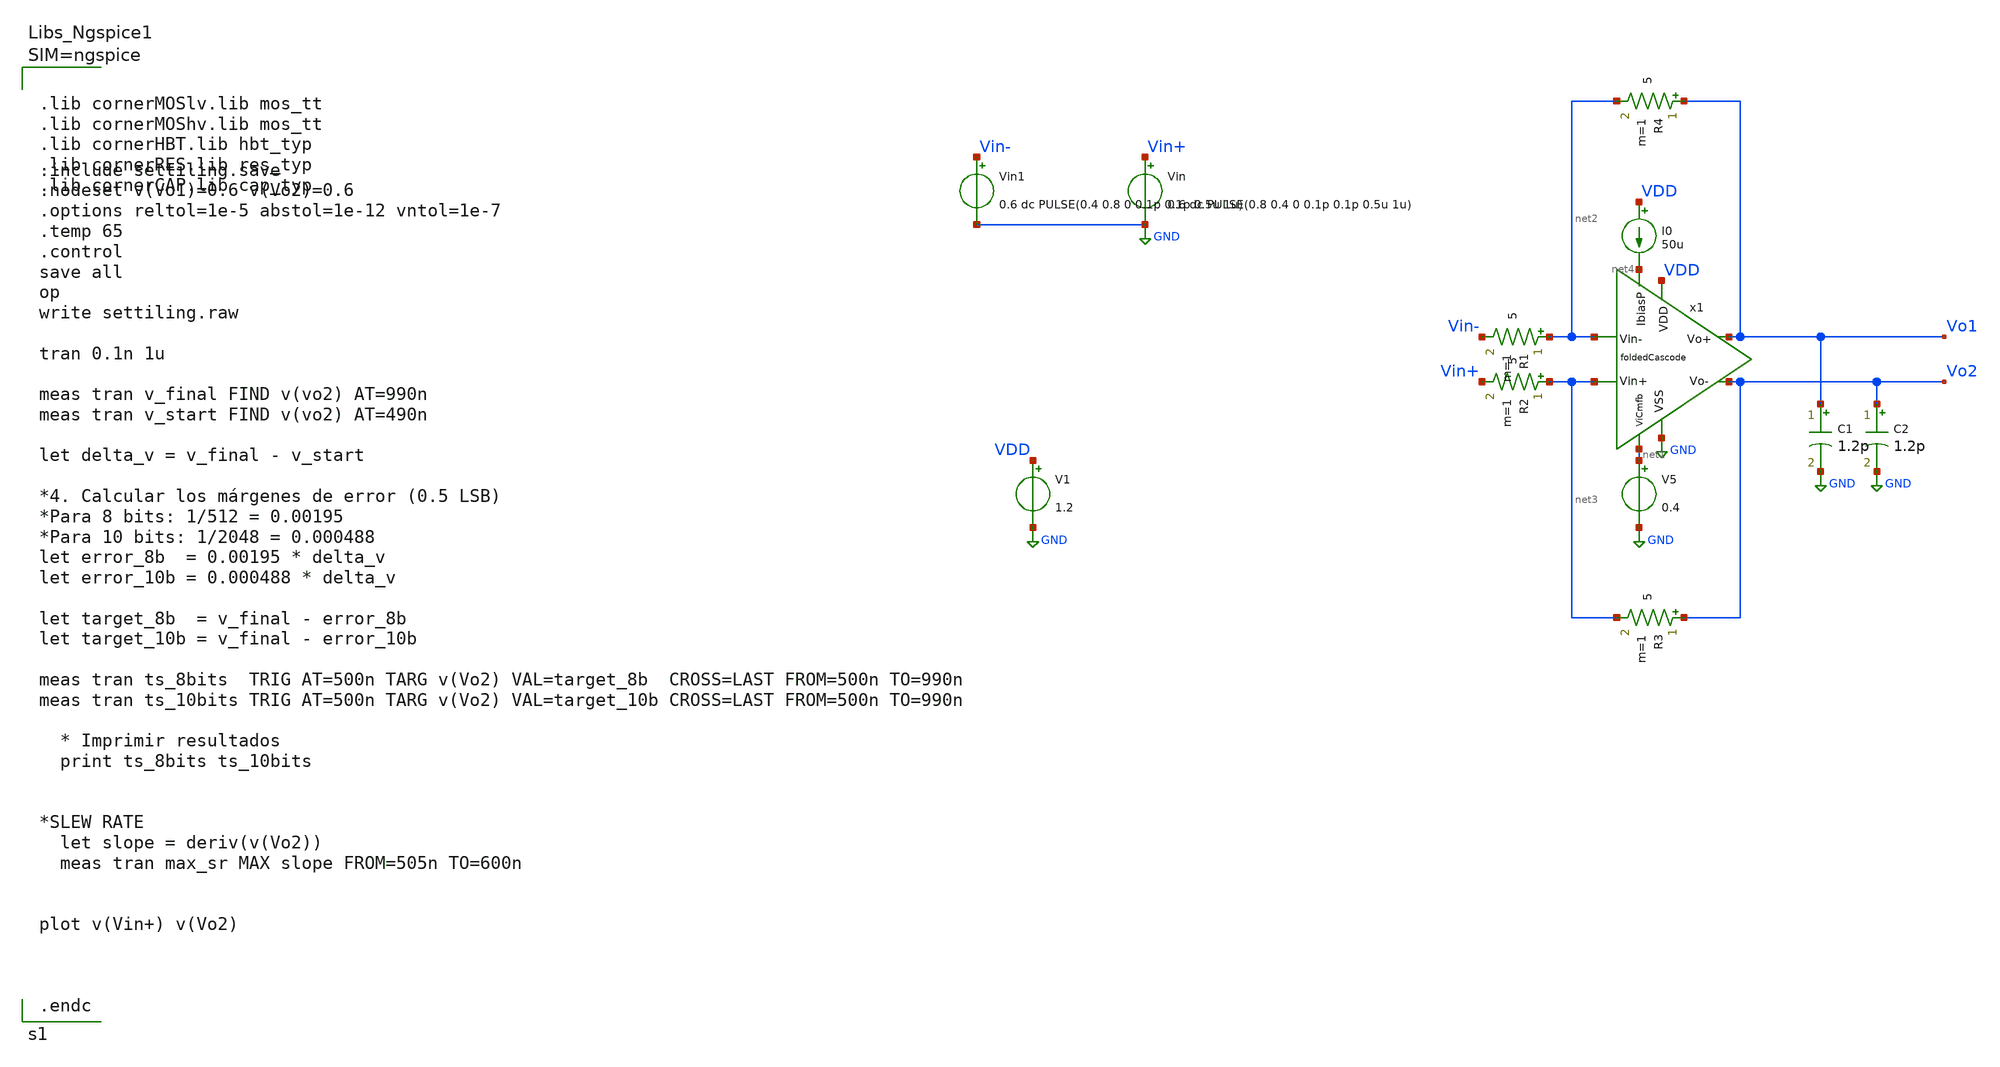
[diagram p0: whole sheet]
** sch_path: sch/tb/settiling.sch
**.subckt settiling
x1 VDD GND net1 net4 Vo1 Vo2 net2 net3 foldedCascode
V1 VDD GND 1.2
I0 VDD net4 50u
C1 Vo1 GND 1.2p m=1
C2 Vo2 GND 1.2p m=1
V5 net1 GND 0.4
Vin Vin+ GND 0.6 dc PULSE(0.8 0.4 0 0.1p 0.1p 0.5u 1u)
Vin1 Vin- GND 0.6 dc PULSE(0.4 0.8 0 0.1p 0.1p 0.5u 1u)
R4 Vo1 net2 5 m=1
R1 net2 Vin- 5 m=1
R2 net3 Vin+ 5 m=1
R3 Vo2 net3 5 m=1
**** begin user architecture code


.include settiling.save
.nodeset v(Vo1)=0.6 v(Vo2)=0.6
.options reltol=1e-5 abstol=1e-12 vntol=1e-7
.temp 65
.control
save all
op
write settiling.raw

tran 0.1n 1u

meas tran v_final FIND v(vo2) AT=990n
meas tran v_start FIND v(vo2) AT=490n

let delta_v = v_final - v_start

*4. Calcular los márgenes de error (0.5 LSB)
*Para 8 bits: 1/512 = 0.00195
*Para 10 bits: 1/2048 = 0.000488
let error_8b  = 0.00195 * delta_v
let error_10b = 0.000488 * delta_v

let target_8b  = v_final - error_8b
let target_10b = v_final - error_10b

meas tran ts_8bits  TRIG AT=500n TARG v(Vo2) VAL=target_8b  CROSS=LAST FROM=500n TO=990n
meas tran ts_10bits TRIG AT=500n TARG v(Vo2) VAL=target_10b CROSS=LAST FROM=500n TO=990n

  * Imprimir resultados
  print ts_8bits ts_10bits


*SLEW RATE
  let slope = deriv(v(Vo2))
  meas tran max_sr MAX slope FROM=505n TO=600n


plot v(Vin+) v(Vo2)



.endc





.lib cornerMOSlv.lib mos_tt
.lib cornerMOShv.lib mos_tt
.lib cornerHBT.lib hbt_typ
.lib cornerRES.lib res_typ
.lib cornerCAP.lib cap_typ



**** end user architecture code
**.ends

* expanding   symbol:  foldedCascode.sym # of pins=8
** sym_path: sch/blocks/foldedCascode.sym
** sch_path: sch/blocks/foldedCascode.sch
.subckt foldedCascode VDD VSS ViCmfb IbiasP Vo+ Vo- Vin- Vin+
*.iopin VSS
*.iopin VDD
*.ipin ViCmfb
*.iopin IbiasP
*.ipin Vin+
*.ipin Vin-
*.iopin Vo+
*.iopin Vo-
XM11 IbiasP IbiasP VSS VSS sg13_lv_nmos w=2u l=0.3u ng=1 m=1 mm_ok=1
x1 VDD Vb1_1 Vb1_2 Vx Vy VSS gmBoosting
XM0 net3 Vb0 VDD VDD sg13_lv_pmos w=70u l=0.3u ng=120 m=8 mm_ok=1
XM14 Vb3 IbiasP VSS VSS sg13_lv_nmos w=0.5u l=0.3u ng=1 m=1 mm_ok=1
XM15 Vb3 Vb3 VDD VDD sg13_lv_pmos w=4.4u l=0.3u ng=2 m=1 mm_ok=1
XM16 net4 IbiasP VSS VSS sg13_lv_nmos w=0.5u l=0.3u ng=1 m=1 mm_ok=1
XM17 net4 net4 VDD VDD sg13_lv_pmos w=9.5u l=0.3u ng=5 m=1 mm_ok=1
XM1 Vy Vin+ net3 net3 sg13_lv_pmos w=70u l=0.13u ng=100 m=2 mm_ok=1
XM2 Vx Vin- net3 net3 sg13_lv_pmos w=70u l=0.13u ng=100 m=2 mm_ok=1
XM9 net1 Vb3 VDD VDD sg13_lv_pmos w=62u l=0.8u ng=120 m=4 mm_ok=1
XM10 net2 Vb3 VDD VDD sg13_lv_pmos w=62u l=0.8u ng=120 m=4 mm_ok=1
XM7 Vo+ Vb2 net1 VDD sg13_lv_pmos w=63u l=0.4u ng=120 m=4 mm_ok=1
XM3 Vo+ Vb1_1 Vx VSS sg13_lv_nmos w=44u l=0.3u ng=18 m=6 mm_ok=1
V10 Vb0 VSS 0.78
V3 Vb1 GND 0.56
V4 Vb2 GND 0.48
V5 Vb3 GND 0.71
XM8 Vo- Vb2 net2 VDD sg13_lv_pmos w=63u l=0.4u ng=120 m=4 mm_ok=1
XM12 Vx ViCmfb VSS VSS sg13_lv_nmos w=24.2u l=0.8u ng=64 m=6 mm_ok=1
XM4 Vo- Vb1_2 Vy VSS sg13_lv_nmos w=44u l=0.3u ng=18 m=6 mm_ok=1
XM5 Vy ViCmfb VSS VSS sg13_lv_nmos w=24.2u l=0.8u ng=64 m=6 mm_ok=1
.ends


* expanding   symbol:  gmBoosting.sym # of pins=6
** sym_path: sch/blocks/gmBoosting.sym
** sch_path: sch/blocks/gmBoosting.sch
.subckt gmBoosting VDD Vo2 Vo1 Vi+ Vi- VSS
*.iopin VSS
*.opin Vo1
*.opin Vo2
*.ipin Vi+
*.ipin Vi-
*.iopin VDD
V1 Vref VSS 0.55
XM7 net2 Vb4 VDD VDD sg13_lv_pmos w=25u l=0.7u ng=13 m=2 mm_ok=1
XM1 net8 Vi+ net1 net1 sg13_lv_pmos w=40u l=0.15u ng=80 m=4 mm_ok=1
XM2 net4 Vi- net1 net1 sg13_lv_pmos w=40u l=0.15u ng=80 m=4 mm_ok=1
XM0 net1 Vb0 net5 VDD sg13_lv_pmos w=16u l=0.3u ng=20 m=1 mm_ok=1
XM6 net8 Vb3 VSS VSS sg13_lv_nmos w=20u l=0.7u ng=5 m=2 mm_ok=1
XM9 Vo1 Vb2 net2 VDD sg13_lv_pmos w=30u l=0.3u ng=10 m=1 mm_ok=1
XM10 Vo2 Vb2 net3 VDD sg13_lv_pmos w=30u l=0.3u ng=10 m=1 mm_ok=1
XM8 net3 Vb4 VDD VDD sg13_lv_pmos w=25u l=0.7u ng=13 m=2 mm_ok=1
XM3 net5 Vo2 VDD VDD sg13_lv_pmos w=20u l=0.13u ng=5 m=1 mm_ok=1
XM4 net5 Vo1 VDD VDD sg13_lv_pmos w=20u l=0.13u ng=5 m=1 mm_ok=1
XM5 net6 Vref VDD VDD sg13_lv_pmos w=20u l=0.13u ng=5 m=2 mm_ok=1
XM28 Vb0 net7 VSS VSS sg13_lv_nmos w=10u l=0.2u ng=2 m=1 mm_ok=1
XM29 Vb3 Vb3 VSS VSS sg13_lv_nmos w=30u l=0.2u ng=4 m=1 mm_ok=1
XR16 net7 Vb0 sub! rppd w=0.8e-6 l=2.5e-6 m=1 b=0 mm_ok=1
XM30 Vb3 Vb0 net6 VDD sg13_lv_pmos w=16u l=0.3u ng=20 m=1 mm_ok=1
XM31 net4 Vb3 VSS VSS sg13_lv_nmos w=20u l=0.7u ng=5 m=2 mm_ok=1
XM32 Vo1 Vb1 net4 VSS sg13_lv_nmos w=37.5u l=0.7u ng=5 m=1 mm_ok=1
XM33 Vo2 Vb1 net8 VSS sg13_lv_nmos w=37.5u l=0.7u ng=5 m=1 mm_ok=1
XM23 net7 Vbb VDD VDD sg13_lv_pmos w=18u l=1u ng=18 m=1 mm_ok=1
XR9 Vb1 net10 sub! rhigh w=0.5e-6 l=2.31e-6 m=1 b=0 mm_ok=1
XM17 net10 Vb1 net9 VSS sg13_lv_nmos w=25u l=0.7u ng=3 m=1 mm_ok=1
XM18 net9 net10 VSS VSS sg13_lv_nmos w=40u l=0.7u ng=4 m=1 mm_ok=1
XM19 net11 Vb4 VDD VDD sg13_lv_pmos w=15u l=0.7u ng=5 m=1 mm_ok=1
XM20 Vb4 Vb2 net11 VDD sg13_lv_pmos w=7u l=0.3u ng=7 m=1 mm_ok=1
XR10 Vb4 Vb2 sub! rhigh w=0.5e-6 l=1.8e-6 m=1 b=0 mm_ok=1
I3 Vbb VSS 50u
XM21 Vbb Vbb VDD VDD sg13_lv_pmos w=18u l=1u ng=18 m=1 mm_ok=1
XM22 Vb1 Vbb VDD VDD sg13_lv_pmos w=18u l=1u ng=18 m=1 mm_ok=1
XM24 net12 Vbb VDD VDD sg13_lv_pmos w=18u l=1u ng=18 m=1 mm_ok=1
XM25 net12 net12 VSS VSS sg13_lv_nmos w=15u l=1u ng=2 m=1 mm_ok=1
XM26 Vb2 net12 VSS VSS sg13_lv_nmos w=15u l=1u ng=2 m=1 mm_ok=1
.ends

.GLOBAL GND
.end
